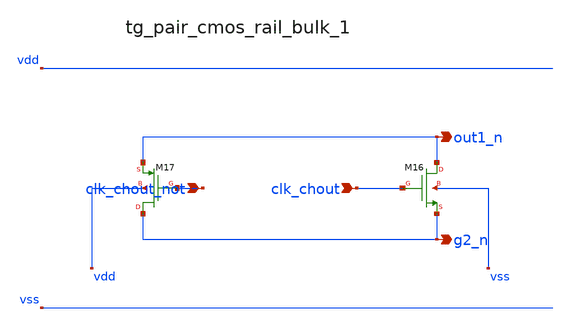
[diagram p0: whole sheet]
** sch_path: analog-db/raw/ia_003_fan_chopper_pf/hier/blocks/tg_pair_cmos_rail_bulk_1.sch
**.subckt tg_pair_cmos_rail_bulk_1 clk_chout_not clk_chout out1_n g2_n
*.ipin clk_chout_not
*.ipin clk_chout
*.opin out1_n
*.opin g2_n
XM16 out1_n clk_chout g2_n vss sg13_lv_nmos w=x_dut_xm16_w l=x_dut_xm16_l ng=1 m=x_dut_xm16_m
XM17 g2_n clk_chout_not out1_n vdd sg13_lv_pmos w=x_dut_xm17_w l=x_dut_xm17_l ng=1 m=x_dut_xm17_m
**.ends
.end
